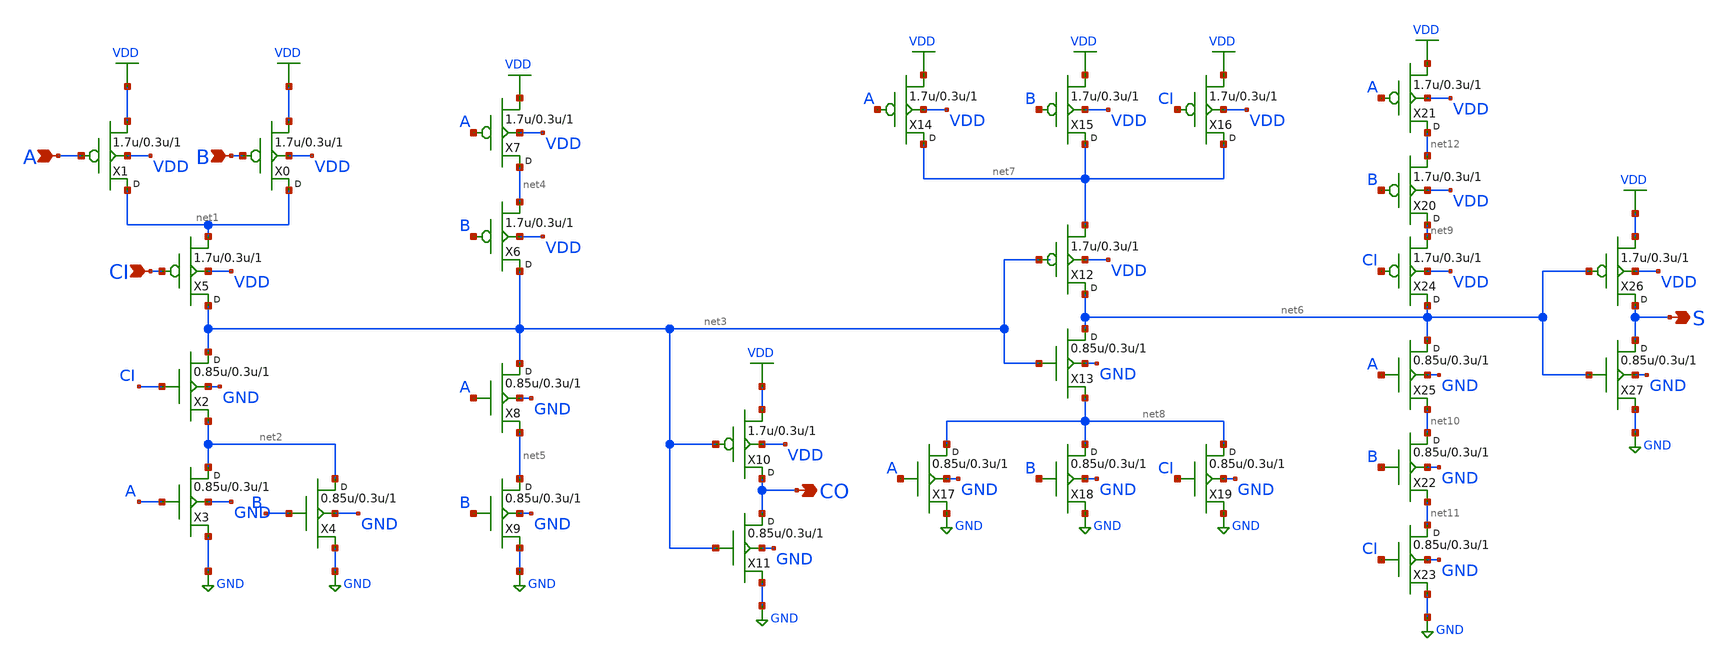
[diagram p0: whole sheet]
** sch_path: lib/xschem/gf180mcu_osu_sc_12T_addf_1.sch
**.subckt gf180mcu_osu_sc_12T_addf_1 A B CI S CO
*.ipin A
*.ipin B
*.ipin CI
*.opin S
*.opin CO
X1 net1 A VDD VDD pmos_3p3 w=1.7u l=0.3u m=1
X0 net1 B VDD VDD pmos_3p3 w=1.7u l=0.3u m=1
X2 net3 CI net2 GND nmos_3p3 w=0.85u l=0.3u m=1
X3 net2 A GND GND nmos_3p3 w=0.85u l=0.3u m=1
X4 net2 B GND GND nmos_3p3 w=0.85u l=0.3u m=1
X5 net3 CI net1 VDD pmos_3p3 w=1.7u l=0.3u m=1
X6 net3 B net4 VDD pmos_3p3 w=1.7u l=0.3u m=1
X7 net4 A VDD VDD pmos_3p3 w=1.7u l=0.3u m=1
X8 net3 A net5 GND nmos_3p3 w=0.85u l=0.3u m=1
X9 net5 B GND GND nmos_3p3 w=0.85u l=0.3u m=1
X10 CO net3 VDD VDD pmos_3p3 w=1.7u l=0.3u m=1
X11 CO net3 GND GND nmos_3p3 w=0.85u l=0.3u m=1
X12 net6 net3 net7 VDD pmos_3p3 w=1.7u l=0.3u m=1
X13 net6 net3 net8 GND nmos_3p3 w=0.85u l=0.3u m=1
X14 net7 A VDD VDD pmos_3p3 w=1.7u l=0.3u m=1
X15 net7 B VDD VDD pmos_3p3 w=1.7u l=0.3u m=1
X16 net7 CI VDD VDD pmos_3p3 w=1.7u l=0.3u m=1
X17 net8 A GND GND nmos_3p3 w=0.85u l=0.3u m=1
X18 net8 B GND GND nmos_3p3 w=0.85u l=0.3u m=1
X19 net8 CI GND GND nmos_3p3 w=0.85u l=0.3u m=1
X20 net9 B net12 VDD pmos_3p3 w=1.7u l=0.3u m=1
X21 net12 A VDD VDD pmos_3p3 w=1.7u l=0.3u m=1
X22 net10 B net11 GND nmos_3p3 w=0.85u l=0.3u m=1
X23 net11 CI GND GND nmos_3p3 w=0.85u l=0.3u m=1
X24 net6 CI net9 VDD pmos_3p3 w=1.7u l=0.3u m=1
X25 net6 A net10 GND nmos_3p3 w=0.85u l=0.3u m=1
X26 S net6 VDD VDD pmos_3p3 w=1.7u l=0.3u m=1
X27 S net6 GND GND nmos_3p3 w=0.85u l=0.3u m=1
**** begin user architecture code


.inc "/import/yukari1/lrburle/OSU_180/char/techfiles/design.hspice"
.lib "/import/yukari1/lrburle/OSU_180/char/techfiles/sm141064.hspice" typical


**** end user architecture code
**.ends
.GLOBAL VDD
.GLOBAL GND
.end
